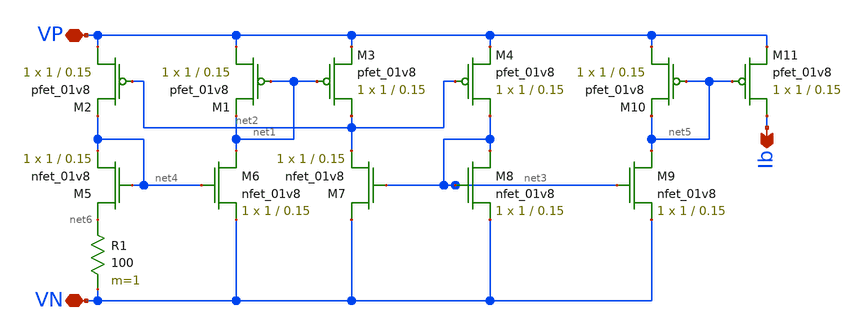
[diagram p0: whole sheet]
** sch_path: schematics/bias_generator.sch
**.subckt bias_generator VP VN Ib
*.iopin VP
*.iopin VN
*.opin Ib
XM2 VP net2 net4 VDD sky130_fd_pr__pfet_01v8 L=0.15 W=1 nf=1 ad='int((nf+1)/2) * W/nf * 0.29' as='int((nf+2)/2) * W/nf * 0.29'
+ pd='2*int((nf+1)/2) * (W/nf + 0.29)' ps='2*int((nf+2)/2) * (W/nf + 0.29)' nrd='0.29 / W' nrs='0.29 / W'
+ sa=0 sb=0 sd=0 mult=1 m=1
XM1 VP net1 net1 VDD sky130_fd_pr__pfet_01v8 L=0.15 W=1 nf=1 ad='int((nf+1)/2) * W/nf * 0.29' as='int((nf+2)/2) * W/nf * 0.29'
+ pd='2*int((nf+1)/2) * (W/nf + 0.29)' ps='2*int((nf+2)/2) * (W/nf + 0.29)' nrd='0.29 / W' nrs='0.29 / W'
+ sa=0 sb=0 sd=0 mult=1 m=1
XM3 net2 net1 VP VDD sky130_fd_pr__pfet_01v8 L=0.15 W=1 nf=1 ad='int((nf+1)/2) * W/nf * 0.29' as='int((nf+2)/2) * W/nf * 0.29'
+ pd='2*int((nf+1)/2) * (W/nf + 0.29)' ps='2*int((nf+2)/2) * (W/nf + 0.29)' nrd='0.29 / W' nrs='0.29 / W'
+ sa=0 sb=0 sd=0 mult=1 m=1
XM4 net3 net2 VP VDD sky130_fd_pr__pfet_01v8 L=0.15 W=1 nf=1 ad='int((nf+1)/2) * W/nf * 0.29' as='int((nf+2)/2) * W/nf * 0.29'
+ pd='2*int((nf+1)/2) * (W/nf + 0.29)' ps='2*int((nf+2)/2) * (W/nf + 0.29)' nrd='0.29 / W' nrs='0.29 / W'
+ sa=0 sb=0 sd=0 mult=1 m=1
XM5 net6 net4 net4 GND sky130_fd_pr__nfet_01v8 L=0.15 W=1 nf=1 ad='int((nf+1)/2) * W/nf * 0.29' as='int((nf+2)/2) * W/nf * 0.29'
+ pd='2*int((nf+1)/2) * (W/nf + 0.29)' ps='2*int((nf+2)/2) * (W/nf + 0.29)' nrd='0.29 / W' nrs='0.29 / W'
+ sa=0 sb=0 sd=0 mult=1 m=1
XM6 net1 net4 VN GND sky130_fd_pr__nfet_01v8 L=0.15 W=1 nf=1 ad='int((nf+1)/2) * W/nf * 0.29' as='int((nf+2)/2) * W/nf * 0.29'
+ pd='2*int((nf+1)/2) * (W/nf + 0.29)' ps='2*int((nf+2)/2) * (W/nf + 0.29)' nrd='0.29 / W' nrs='0.29 / W'
+ sa=0 sb=0 sd=0 mult=1 m=1
XM7 VN net3 net2 GND sky130_fd_pr__nfet_01v8 L=0.15 W=1 nf=1 ad='int((nf+1)/2) * W/nf * 0.29' as='int((nf+2)/2) * W/nf * 0.29'
+ pd='2*int((nf+1)/2) * (W/nf + 0.29)' ps='2*int((nf+2)/2) * (W/nf + 0.29)' nrd='0.29 / W' nrs='0.29 / W'
+ sa=0 sb=0 sd=0 mult=1 m=1
XM8 net3 net3 VN GND sky130_fd_pr__nfet_01v8 L=0.15 W=1 nf=1 ad='int((nf+1)/2) * W/nf * 0.29' as='int((nf+2)/2) * W/nf * 0.29'
+ pd='2*int((nf+1)/2) * (W/nf + 0.29)' ps='2*int((nf+2)/2) * (W/nf + 0.29)' nrd='0.29 / W' nrs='0.29 / W'
+ sa=0 sb=0 sd=0 mult=1 m=1
R1 net6 VN 100 m=1
XM9 net5 net3 VN GND sky130_fd_pr__nfet_01v8 L=0.15 W=1 nf=1 ad='int((nf+1)/2) * W/nf * 0.29' as='int((nf+2)/2) * W/nf * 0.29'
+ pd='2*int((nf+1)/2) * (W/nf + 0.29)' ps='2*int((nf+2)/2) * (W/nf + 0.29)' nrd='0.29 / W' nrs='0.29 / W'
+ sa=0 sb=0 sd=0 mult=1 m=1
XM10 VP net5 net5 VDD sky130_fd_pr__pfet_01v8 L=0.15 W=1 nf=1 ad='int((nf+1)/2) * W/nf * 0.29' as='int((nf+2)/2) * W/nf * 0.29'
+ pd='2*int((nf+1)/2) * (W/nf + 0.29)' ps='2*int((nf+2)/2) * (W/nf + 0.29)' nrd='0.29 / W' nrs='0.29 / W'
+ sa=0 sb=0 sd=0 mult=1 m=1
XM11 Ib net5 VP VDD sky130_fd_pr__pfet_01v8 L=0.15 W=1 nf=1 ad='int((nf+1)/2) * W/nf * 0.29' as='int((nf+2)/2) * W/nf * 0.29'
+ pd='2*int((nf+1)/2) * (W/nf + 0.29)' ps='2*int((nf+2)/2) * (W/nf + 0.29)' nrd='0.29 / W' nrs='0.29 / W'
+ sa=0 sb=0 sd=0 mult=1 m=1
**.ends
.end
